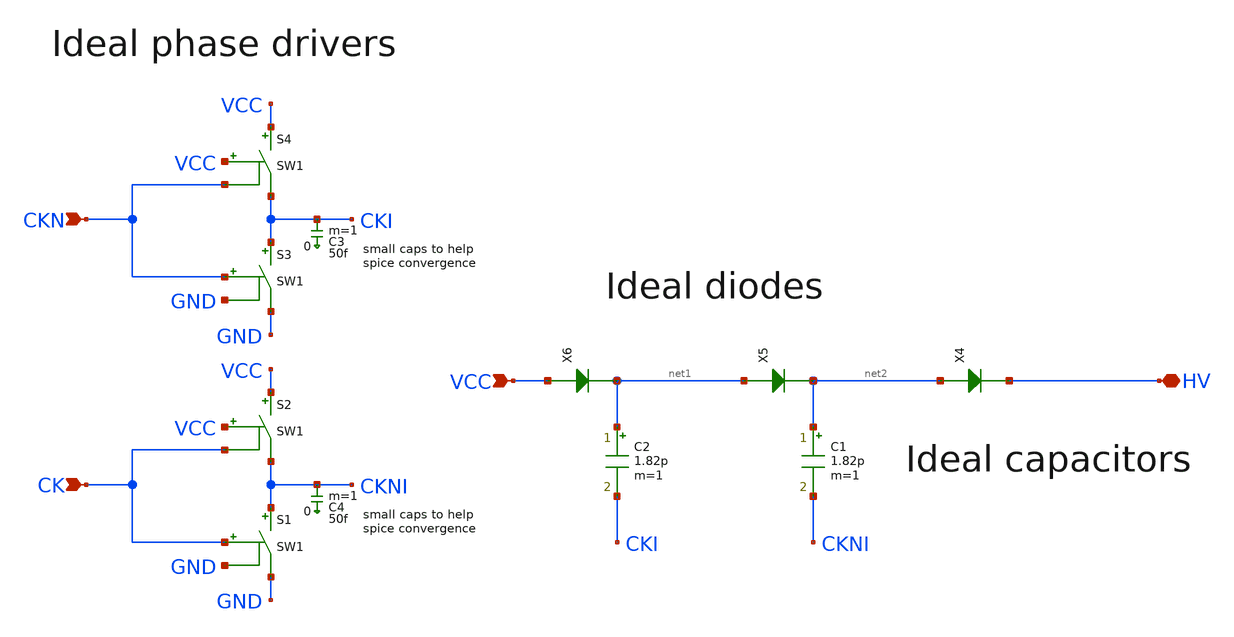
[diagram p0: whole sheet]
** sch_path: sky130_tests/charge_pump_ideal.sch
* Copyright 2021 Stefan Frederik Schippers
* Licensed under the Apache License, Version 2.0 (the "License");
* you may not use this file except in compliance with the License.
* You may obtain a copy of the License at
* https://www.apache.org/licenses/LICENSE-2.0
* Unless required by applicable law or agreed to in writing, software
* distributed under the License is distributed on an "AS IS" BASIS,
* WITHOUT WARRANTIES OR CONDITIONS OF ANY KIND, either express or implied.
* See the License for the specific language governing permissions and
* limitations under the License.
**.subckt charge_pump_ideal HV VCC CK CKN
*.iopin HV
*.ipin VCC
*.ipin CK
*.ipin CKN
X4 net2 HV diode_ngspice Ron=0.1 Roff=1e9 m=1
X5 net1 net2 diode_ngspice Ron=0.1 Roff=1e9 m=1
X6 VCC net1 diode_ngspice Ron=0.1 Roff=1e9 m=1
C1 net2 CKNI 1.82p m=1
C2 net1 CKI 1.82p m=1
S1 CKNI GND CK GND SW1
S2 VCC CKNI VCC CK SW1
S3 CKI GND CKN GND SW1
S4 VCC CKI VCC CKN SW1
C3 CKI 0 50f m=1
C4 CKNI 0 50f m=1
**.ends

* expanding   symbol:  sky130_tests/diode_ngspice.sym # of pins=2
** sym_path: sky130_tests/diode_ngspice.sym
** sch_path: sky130_tests/diode_ngspice.sch
.subckt diode_ngspice plus minus   Roff=1e9 Ron=0.1
*.iopin plus
*.iopin minus
Vm mn minus 0
.save i(vm)
Vp plus pn 0
.save i(vp)
B1 pn mn I = 'v(pn,mn) > 0 ? v(pn,mn) / Ron : v(pn,mn) / Roff'
.ends

**** begin user architecture code
.MODEL SW1 SW   VT=1.0 VH=0.01  RON=10 ROFF=10MEG
**** end user architecture code
.end
